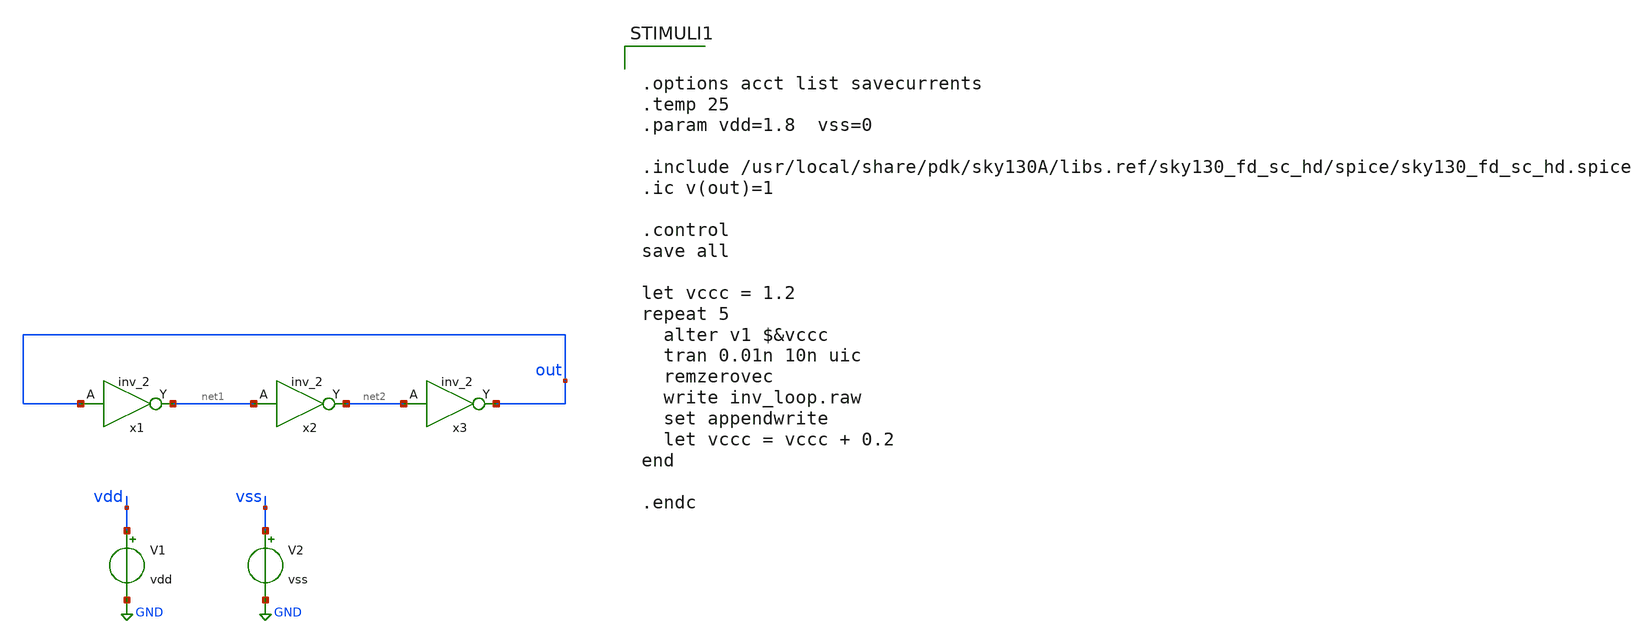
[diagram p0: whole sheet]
** sch_path: xschem/vco/inv_loop.sch
**.subckt inv_loop
x1 out VSS VSS VDD VDD net1 sky130_fd_sc_hd__inv_2
x2 net1 VSS VSS VDD VDD net2 sky130_fd_sc_hd__inv_2
x3 net2 VSS VSS VDD VDD out sky130_fd_sc_hd__inv_2
V1 vdd GND vdd
V2 vss GND vss
**** begin user architecture code

** opencircuitdesign pdks install
.lib $::SKYWATER_MODELS/sky130.lib.spice tt




.options acct list savecurrents
.temp 25
.param vdd=1.8  vss=0

.include /usr/local/share/pdk/sky130A/libs.ref/sky130_fd_sc_hd/spice/sky130_fd_sc_hd.spice
.ic v(out)=1

.control
save all

let vccc = 1.2
repeat 5
  alter v1 $&vccc
  tran 0.01n 10n uic
  remzerovec
  write inv_loop.raw
  set appendwrite
  let vccc = vccc + 0.2
end

.endc


**** end user architecture code
**.ends
.GLOBAL GND
.end
